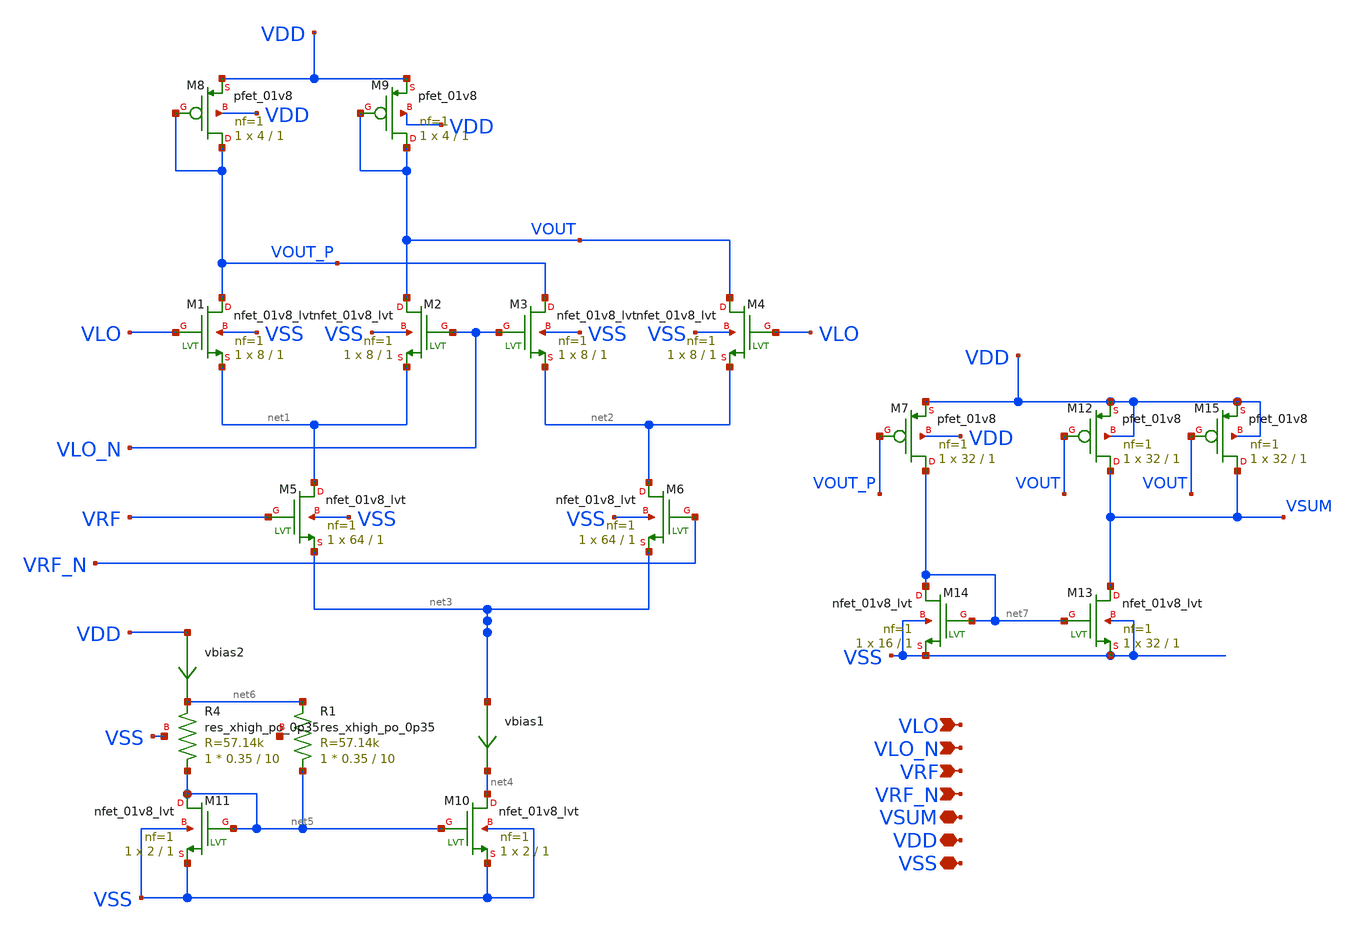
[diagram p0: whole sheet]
** sch_path: tt_um_emilian_rf_playground/xschem/gilbert_mixer.sch
**.subckt gilbert_mixer VSUM VSS VRF_N VRF VLO_N VLO VDD
*.iopin VSUM
*.iopin VSS
*.ipin VRF_N
*.ipin VRF
*.ipin VLO_N
*.ipin VLO
*.iopin VDD
XM1 VOUT_P VLO net1 VSS sky130_fd_pr__nfet_01v8_lvt L=1 W=8 nf=1 ad='int((nf+1)/2) * W/nf * 0.29' as='int((nf+2)/2) * W/nf * 0.29'
+ pd='2*int((nf+1)/2) * (W/nf + 0.29)' ps='2*int((nf+2)/2) * (W/nf + 0.29)' nrd='0.29 / W' nrs='0.29 / W'
+ sa=0 sb=0 sd=0 mult=1 m=1
XM2 VOUT VLO_N net1 VSS sky130_fd_pr__nfet_01v8_lvt L=1 W=8 nf=1 ad='int((nf+1)/2) * W/nf * 0.29' as='int((nf+2)/2) * W/nf * 0.29'
+ pd='2*int((nf+1)/2) * (W/nf + 0.29)' ps='2*int((nf+2)/2) * (W/nf + 0.29)' nrd='0.29 / W' nrs='0.29 / W'
+ sa=0 sb=0 sd=0 mult=1 m=1
XM3 VOUT_P VLO_N net2 VSS sky130_fd_pr__nfet_01v8_lvt L=1 W=8 nf=1 ad='int((nf+1)/2) * W/nf * 0.29' as='int((nf+2)/2) * W/nf * 0.29'
+ pd='2*int((nf+1)/2) * (W/nf + 0.29)' ps='2*int((nf+2)/2) * (W/nf + 0.29)' nrd='0.29 / W' nrs='0.29 / W'
+ sa=0 sb=0 sd=0 mult=1 m=1
XM4 VOUT VLO net2 VSS sky130_fd_pr__nfet_01v8_lvt L=1 W=8 nf=1 ad='int((nf+1)/2) * W/nf * 0.29' as='int((nf+2)/2) * W/nf * 0.29'
+ pd='2*int((nf+1)/2) * (W/nf + 0.29)' ps='2*int((nf+2)/2) * (W/nf + 0.29)' nrd='0.29 / W' nrs='0.29 / W'
+ sa=0 sb=0 sd=0 mult=1 m=1
XM5 net1 VRF net3 VSS sky130_fd_pr__nfet_01v8_lvt L=1 W=64 nf=1 ad='int((nf+1)/2) * W/nf * 0.29' as='int((nf+2)/2) * W/nf * 0.29'
+ pd='2*int((nf+1)/2) * (W/nf + 0.29)' ps='2*int((nf+2)/2) * (W/nf + 0.29)' nrd='0.29 / W' nrs='0.29 / W'
+ sa=0 sb=0 sd=0 mult=1 m=1
XM6 net2 VRF_N net3 VSS sky130_fd_pr__nfet_01v8_lvt L=1 W=64 nf=1 ad='int((nf+1)/2) * W/nf * 0.29' as='int((nf+2)/2) * W/nf * 0.29'
+ pd='2*int((nf+1)/2) * (W/nf + 0.29)' ps='2*int((nf+2)/2) * (W/nf + 0.29)' nrd='0.29 / W' nrs='0.29 / W'
+ sa=0 sb=0 sd=0 mult=1 m=1
XM8 VOUT_P VOUT_P VDD VDD sky130_fd_pr__pfet_01v8 L=1 W=4 nf=1 ad='int((nf+1)/2) * W/nf * 0.29' as='int((nf+2)/2) * W/nf * 0.29'
+ pd='2*int((nf+1)/2) * (W/nf + 0.29)' ps='2*int((nf+2)/2) * (W/nf + 0.29)' nrd='0.29 / W' nrs='0.29 / W'
+ sa=0 sb=0 sd=0 mult=1 m=1
XM9 VOUT VOUT VDD VDD sky130_fd_pr__pfet_01v8 L=1 W=4 nf=1 ad='int((nf+1)/2) * W/nf * 0.29' as='int((nf+2)/2) * W/nf * 0.29'
+ pd='2*int((nf+1)/2) * (W/nf + 0.29)' ps='2*int((nf+2)/2) * (W/nf + 0.29)' nrd='0.29 / W' nrs='0.29 / W'
+ sa=0 sb=0 sd=0 mult=1 m=1
XM10 net4 net5 VSS VSS sky130_fd_pr__nfet_01v8_lvt L=1 W=2 nf=1 ad='int((nf+1)/2) * W/nf * 0.29' as='int((nf+2)/2) * W/nf * 0.29'
+ pd='2*int((nf+1)/2) * (W/nf + 0.29)' ps='2*int((nf+2)/2) * (W/nf + 0.29)' nrd='0.29 / W' nrs='0.29 / W'
+ sa=0 sb=0 sd=0 mult=1 m=1
vbias1 net3 net4 0
.save i(vbias1)
XM11 net5 net5 VSS VSS sky130_fd_pr__nfet_01v8_lvt L=1 W=2 nf=1 ad='int((nf+1)/2) * W/nf * 0.29' as='int((nf+2)/2) * W/nf * 0.29'
+ pd='2*int((nf+1)/2) * (W/nf + 0.29)' ps='2*int((nf+2)/2) * (W/nf + 0.29)' nrd='0.29 / W' nrs='0.29 / W'
+ sa=0 sb=0 sd=0 mult=1 m=1
vbias2 VDD net6 0
.save i(vbias2)
XR4 net5 net6 VSS sky130_fd_pr__res_xhigh_po_0p35 L=10 mult=1 m=1
XR1 net5 net6 net8 sky130_fd_pr__res_xhigh_po_0p35 L=10 mult=1 m=1
XM7 net7 VOUT_P VDD VDD sky130_fd_pr__pfet_01v8 L=1 W=32 nf=1 ad='int((nf+1)/2) * W/nf * 0.29' as='int((nf+2)/2) * W/nf * 0.29'
+ pd='2*int((nf+1)/2) * (W/nf + 0.29)' ps='2*int((nf+2)/2) * (W/nf + 0.29)' nrd='0.29 / W' nrs='0.29 / W'
+ sa=0 sb=0 sd=0 mult=1 m=1
XM12 VSUM VOUT VDD VDD sky130_fd_pr__pfet_01v8 L=1 W=32 nf=1 ad='int((nf+1)/2) * W/nf * 0.29' as='int((nf+2)/2) * W/nf * 0.29'
+ pd='2*int((nf+1)/2) * (W/nf + 0.29)' ps='2*int((nf+2)/2) * (W/nf + 0.29)' nrd='0.29 / W' nrs='0.29 / W'
+ sa=0 sb=0 sd=0 mult=1 m=1
XM13 VSUM net7 VSS VSS sky130_fd_pr__nfet_01v8_lvt L=1 W=32 nf=1 ad='int((nf+1)/2) * W/nf * 0.29' as='int((nf+2)/2) * W/nf * 0.29'
+ pd='2*int((nf+1)/2) * (W/nf + 0.29)' ps='2*int((nf+2)/2) * (W/nf + 0.29)' nrd='0.29 / W' nrs='0.29 / W'
+ sa=0 sb=0 sd=0 mult=1 m=1
XM14 net7 net7 VSS VSS sky130_fd_pr__nfet_01v8_lvt L=1 W=16 nf=1 ad='int((nf+1)/2) * W/nf * 0.29' as='int((nf+2)/2) * W/nf * 0.29'
+ pd='2*int((nf+1)/2) * (W/nf + 0.29)' ps='2*int((nf+2)/2) * (W/nf + 0.29)' nrd='0.29 / W' nrs='0.29 / W'
+ sa=0 sb=0 sd=0 mult=1 m=1
XM15 VSUM VOUT VDD VDD sky130_fd_pr__pfet_01v8 L=1 W=32 nf=1 ad='int((nf+1)/2) * W/nf * 0.29' as='int((nf+2)/2) * W/nf * 0.29'
+ pd='2*int((nf+1)/2) * (W/nf + 0.29)' ps='2*int((nf+2)/2) * (W/nf + 0.29)' nrd='0.29 / W' nrs='0.29 / W'
+ sa=0 sb=0 sd=0 mult=1 m=1
**.ends
.end
